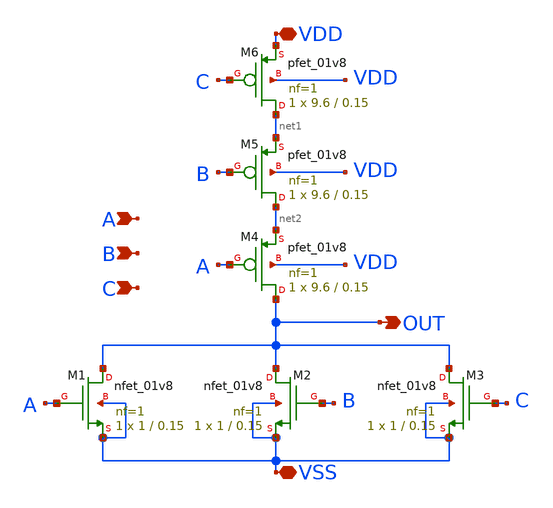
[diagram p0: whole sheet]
** sch_path: design/NOR3/xschem/nor3.sch
**.subckt nor3 A B VSS VDD OUT C
*.ipin A
*.ipin B
*.iopin VSS
*.iopin VDD
*.opin OUT
*.ipin C
XM4 OUT A net2 VDD sky130_fd_pr__pfet_01v8 L=0.15 W=9.6 nf=1 ad='int((nf+1)/2) * W/nf * 0.29' as='int((nf+2)/2) * W/nf * 0.29'
+ pd='2*int((nf+1)/2) * (W/nf + 0.29)' ps='2*int((nf+2)/2) * (W/nf + 0.29)' nrd='0.29 / W' nrs='0.29 / W'
+ sa=0 sb=0 sd=0 mult=1 m=1
XM6 net1 C VDD VDD sky130_fd_pr__pfet_01v8 L=0.15 W=9.6 nf=1 ad='int((nf+1)/2) * W/nf * 0.29' as='int((nf+2)/2) * W/nf * 0.29'
+ pd='2*int((nf+1)/2) * (W/nf + 0.29)' ps='2*int((nf+2)/2) * (W/nf + 0.29)' nrd='0.29 / W' nrs='0.29 / W'
+ sa=0 sb=0 sd=0 mult=1 m=1
XM1 OUT A VSS VSS sky130_fd_pr__nfet_01v8 L=0.15 W=1 nf=1 ad='int((nf+1)/2) * W/nf * 0.29' as='int((nf+2)/2) * W/nf * 0.29'
+ pd='2*int((nf+1)/2) * (W/nf + 0.29)' ps='2*int((nf+2)/2) * (W/nf + 0.29)' nrd='0.29 / W' nrs='0.29 / W'
+ sa=0 sb=0 sd=0 mult=1 m=1
XM2 OUT B VSS VSS sky130_fd_pr__nfet_01v8 L=0.15 W=1 nf=1 ad='int((nf+1)/2) * W/nf * 0.29' as='int((nf+2)/2) * W/nf * 0.29'
+ pd='2*int((nf+1)/2) * (W/nf + 0.29)' ps='2*int((nf+2)/2) * (W/nf + 0.29)' nrd='0.29 / W' nrs='0.29 / W'
+ sa=0 sb=0 sd=0 mult=1 m=1
XM5 net2 B net1 VDD sky130_fd_pr__pfet_01v8 L=0.15 W=9.6 nf=1 ad='int((nf+1)/2) * W/nf * 0.29' as='int((nf+2)/2) * W/nf * 0.29'
+ pd='2*int((nf+1)/2) * (W/nf + 0.29)' ps='2*int((nf+2)/2) * (W/nf + 0.29)' nrd='0.29 / W' nrs='0.29 / W'
+ sa=0 sb=0 sd=0 mult=1 m=1
XM3 OUT C VSS VSS sky130_fd_pr__nfet_01v8 L=0.15 W=1 nf=1 ad='int((nf+1)/2) * W/nf * 0.29' as='int((nf+2)/2) * W/nf * 0.29'
+ pd='2*int((nf+1)/2) * (W/nf + 0.29)' ps='2*int((nf+2)/2) * (W/nf + 0.29)' nrd='0.29 / W' nrs='0.29 / W'
+ sa=0 sb=0 sd=0 mult=1 m=1
**.ends
.end
